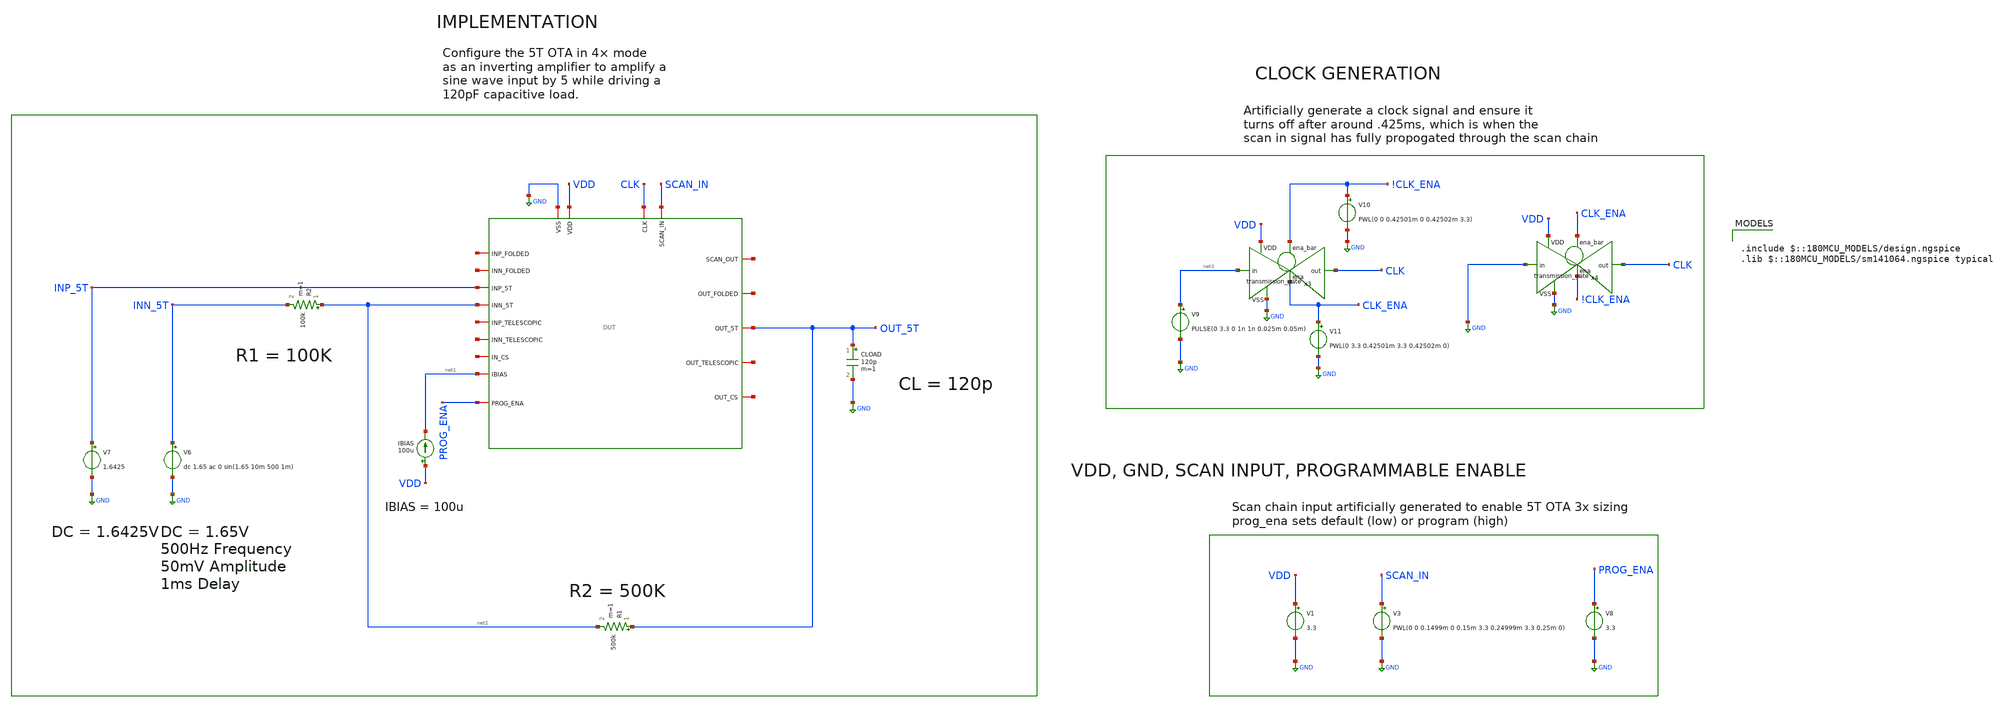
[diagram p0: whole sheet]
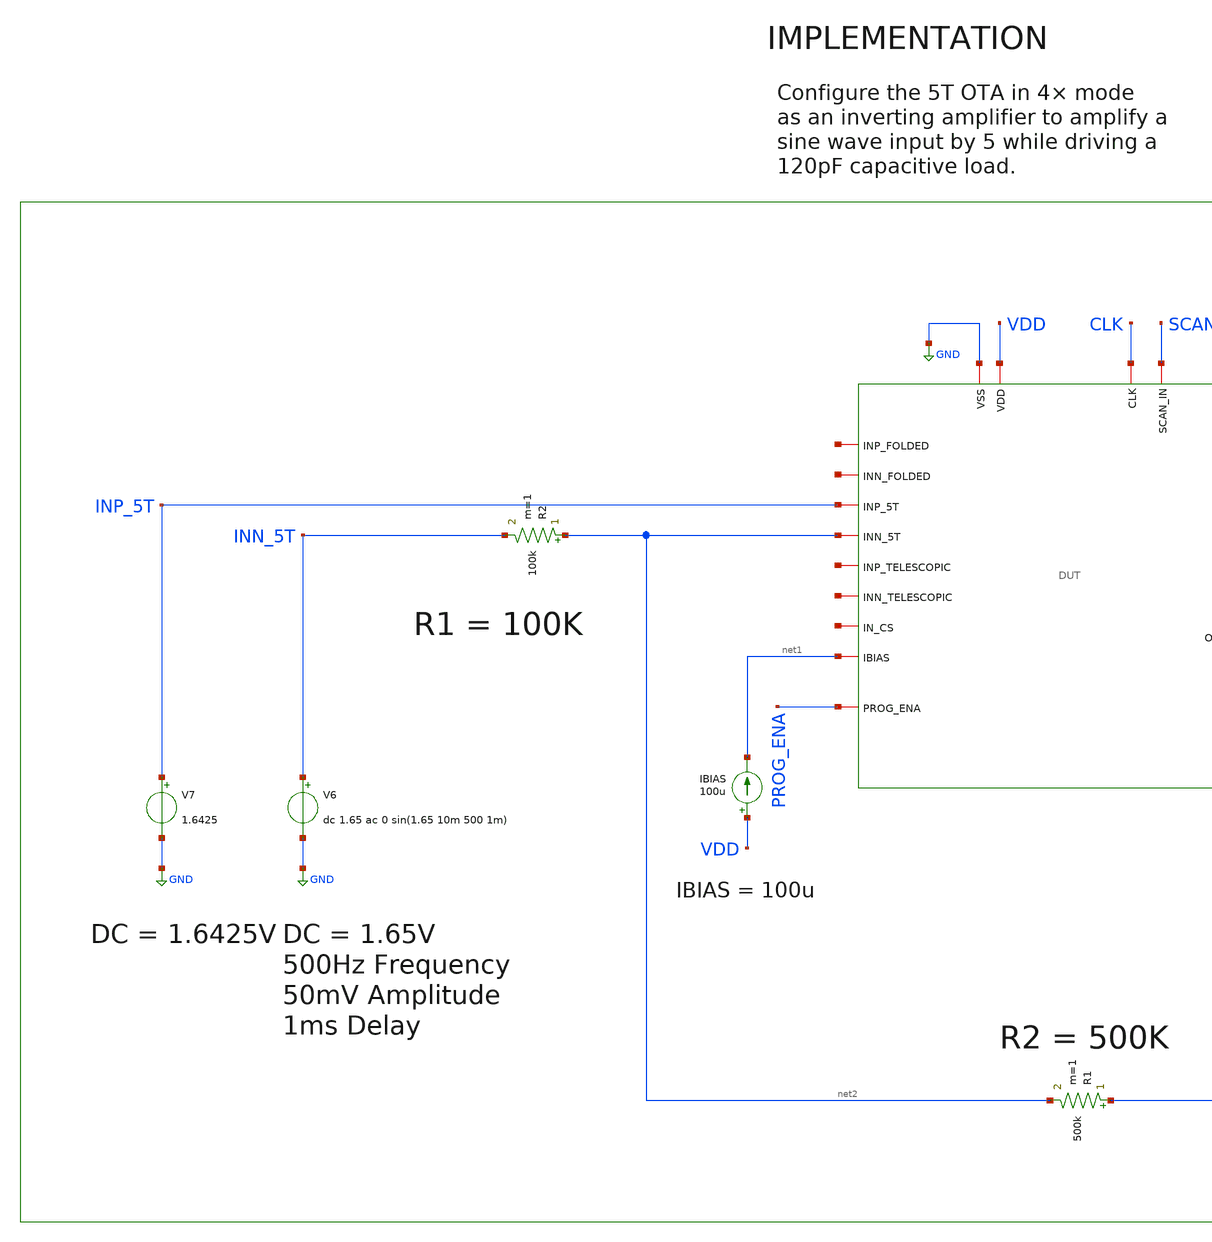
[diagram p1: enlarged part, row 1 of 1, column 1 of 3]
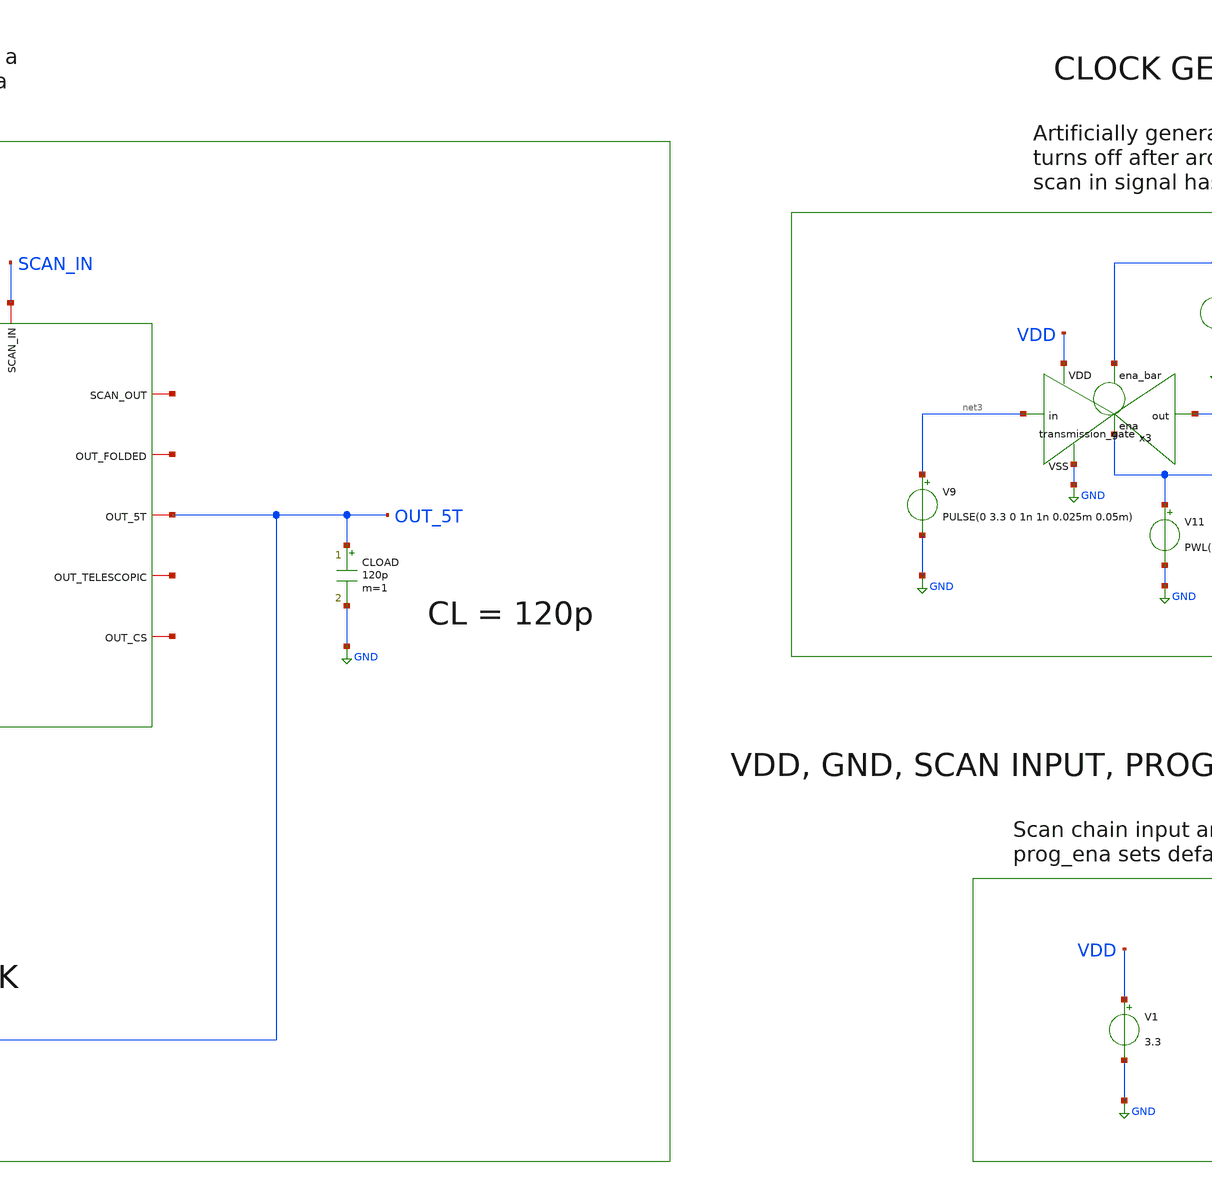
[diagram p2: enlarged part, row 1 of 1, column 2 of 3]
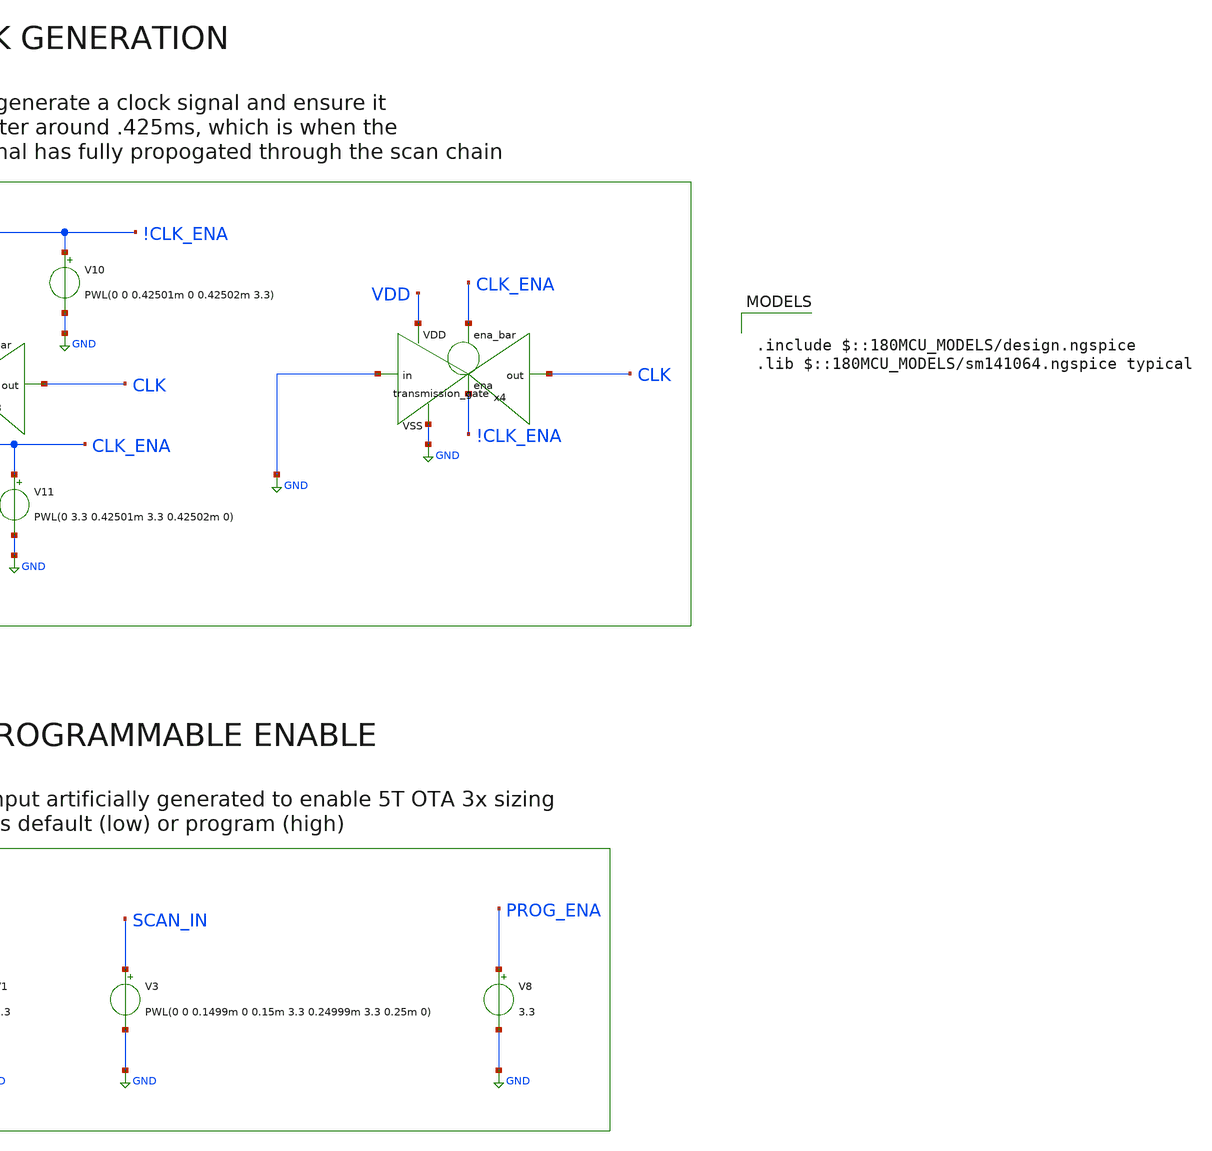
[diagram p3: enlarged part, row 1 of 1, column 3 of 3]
** sch_path: designs/libs/verification/ota_5t/4x_sizing/5t_4x_inverting_amplifier_tb.sch
**.subckt 5t_4x_inverting_amplifier_tb
V3 SCAN_IN GND PWL(0 0 0.1499m 0 0.15m 3.3 0.24999m 3.3 0.25m 0)
V1 VDD GND 3.3
IBIAS VDD net1 100u
V7 INP_5T GND 1.6425
CLOAD OUT_5T GND 120p m=1
R2 net2 INN_5T 100k m=1
V6 INN_5T GND dc 1.65 ac 0 sin(1.65 10m 500 1m)
R1 OUT_5T net2 500k m=1
x1 CLK net4 SCAN_IN GND VDD net5 net6 OUT_5T net1 net7 INP_5T net2 net8 net9 net10 net11 net12
+ PROG_ENA DUT
V8 PROG_ENA GND 3.3
V9 net3 GND PULSE(0 3.3 0 1n 1n 0.025m 0.05m)
x3 !CLK_ENA VDD CLK net3 GND CLK_ENA transmission_gate
V10 !CLK_ENA GND PWL(0 0 0.42501m 0 0.42502m 3.3)
V11 CLK_ENA GND PWL(0 3.3 0.42501m 3.3 0.42502m 0)
x4 CLK_ENA VDD CLK GND GND !CLK_ENA transmission_gate
**** begin user architecture code

.include $::180MCU_MODELS/design.ngspice
.lib $::180MCU_MODELS/sm141064.ngspice typical



.control
tran 1u 5m

set color0 = white
set color1 = black

plot v(out_5T) v(inn_5T)

meas tran vout_pp pp v(out_5T) from=2m to=5m
meas tran vin_pp pp v(inn_5T) from=2m to=5m
let gain = vout_pp / vin_pp
print gain

meas tran vout_dc avg v(out_5T) from=2m to=5m
meas tran vin_dc avg v(inn_5T) from=2m to=5m
let dc_offset = vout_dc - vin_dc
let input_offset = dc_offset / 6
print vout_dc vin_dc dc_offset input_offset

let ideal_gain = 5
let gain_error_pct = (ideal_gain - gain) / ideal_gain * 100
print gain_error_pct

meas tran idd avg i(v1) from=2m to=5m
let power = abs(idd) * 3.3
print idd power
.endc


**** end user architecture code
**.ends
.GLOBAL GND
.end
